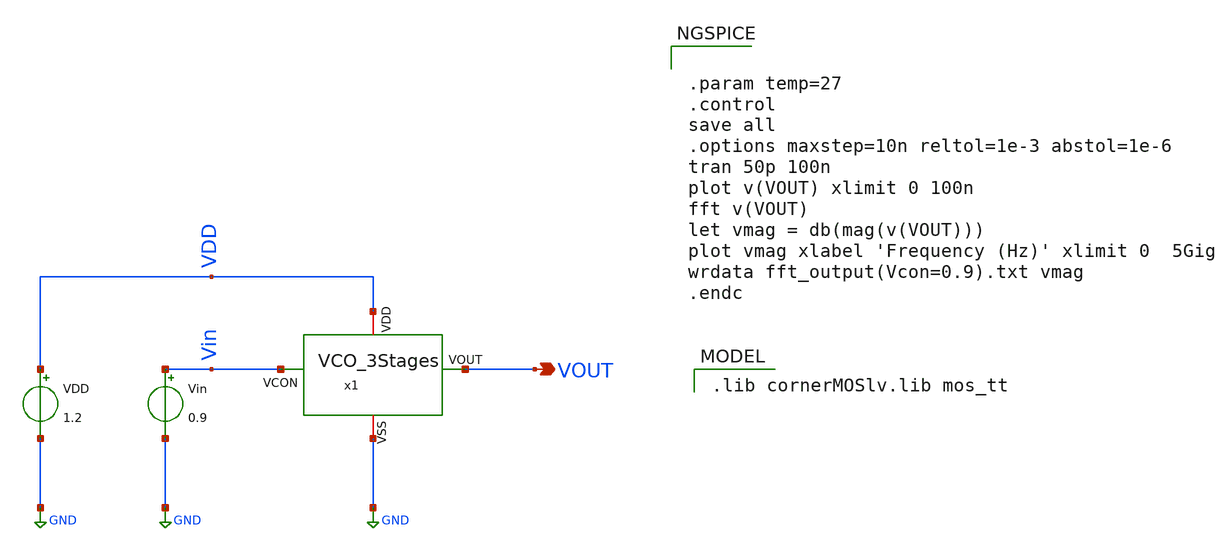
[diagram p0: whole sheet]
** sch_path: Team 1 Design/design_data/xschem/VCO/VCO_3Stages_tb.sch
**.subckt VCO_3Stages_tb VOUT
*.opin VOUT
VDD VDD GND 1.2
Vin Vin GND 0.9
x1 VDD VOUT Vin GND VCO_3Stages
**** begin user architecture code


.param temp=27
.control
save all
.options maxstep=10n reltol=1e-3 abstol=1e-6
tran 50p 100n
plot v(VOUT) xlimit 0 100n
fft v(VOUT)
let vmag = db(mag(v(VOUT)))
plot vmag xlabel 'Frequency (Hz)' xlimit 0  5Gig
wrdata fft_output(Vcon=0.9).txt vmag
.endc


 .lib cornerMOSlv.lib mos_tt

**** end user architecture code
**.ends
.GLOBAL GND
.end
